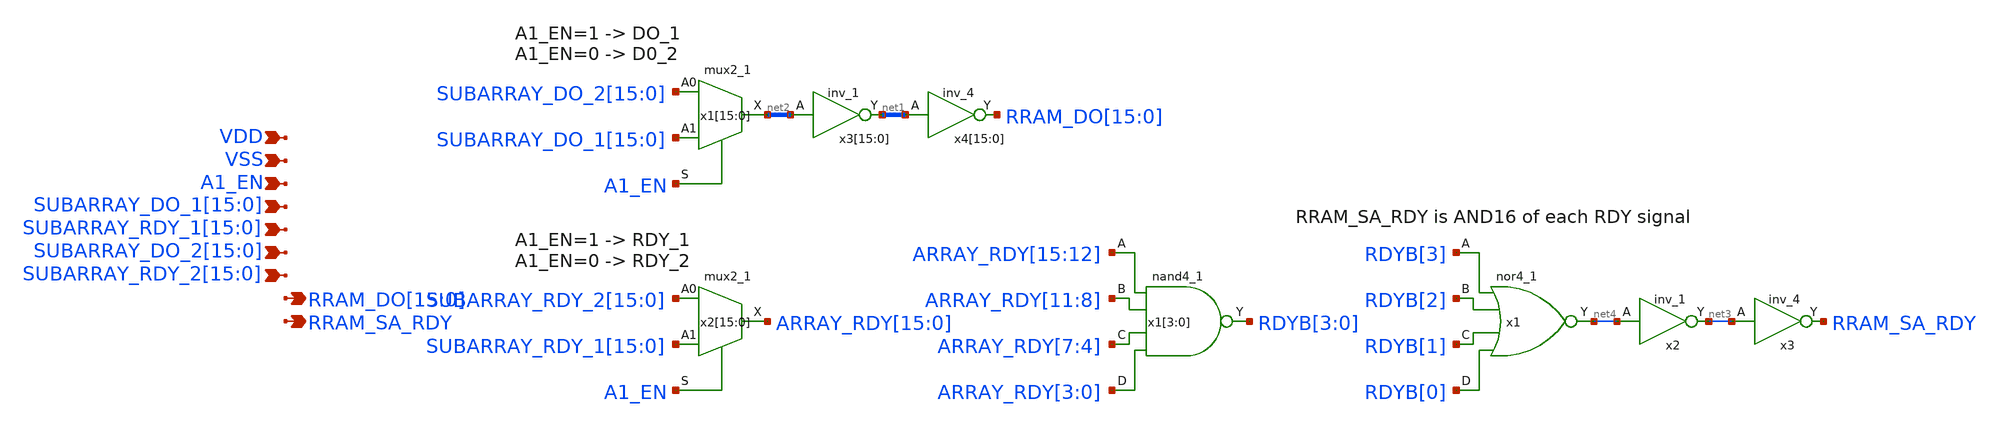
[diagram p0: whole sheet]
** sch_path: Top_Level_Array/array_output_mux.sch
**.subckt array_output_mux VDD VSS A1_EN
*+ SUBARRAY_DO_1[15],SUBARRAY_DO_1[14],SUBARRAY_DO_1[13],SUBARRAY_DO_1[12],SUBARRAY_DO_1[11],SUBARRAY_DO_1[10],SUBARRAY_DO_1[9],SUBARRAY_DO_1[8],SUBARRAY_DO_1[7],SUBARRAY_DO_1[6],SUBARRAY_DO_1[5],SUBARRAY_DO_1[4],SUBARRAY_DO_1[3],SUBARRAY_DO_1[2],SUBARRAY_DO_1[1],SUBARRAY_DO_1[0]
*+ SUBARRAY_RDY_1[15],SUBARRAY_RDY_1[14],SUBARRAY_RDY_1[13],SUBARRAY_RDY_1[12],SUBARRAY_RDY_1[11],SUBARRAY_RDY_1[10],SUBARRAY_RDY_1[9],SUBARRAY_RDY_1[8],SUBARRAY_RDY_1[7],SUBARRAY_RDY_1[6],SUBARRAY_RDY_1[5],SUBARRAY_RDY_1[4],SUBARRAY_RDY_1[3],SUBARRAY_RDY_1[2],SUBARRAY_RDY_1[1],SUBARRAY_RDY_1[0]
*+ SUBARRAY_DO_2[15],SUBARRAY_DO_2[14],SUBARRAY_DO_2[13],SUBARRAY_DO_2[12],SUBARRAY_DO_2[11],SUBARRAY_DO_2[10],SUBARRAY_DO_2[9],SUBARRAY_DO_2[8],SUBARRAY_DO_2[7],SUBARRAY_DO_2[6],SUBARRAY_DO_2[5],SUBARRAY_DO_2[4],SUBARRAY_DO_2[3],SUBARRAY_DO_2[2],SUBARRAY_DO_2[1],SUBARRAY_DO_2[0]
*+ SUBARRAY_RDY_2[15],SUBARRAY_RDY_2[14],SUBARRAY_RDY_2[13],SUBARRAY_RDY_2[12],SUBARRAY_RDY_2[11],SUBARRAY_RDY_2[10],SUBARRAY_RDY_2[9],SUBARRAY_RDY_2[8],SUBARRAY_RDY_2[7],SUBARRAY_RDY_2[6],SUBARRAY_RDY_2[5],SUBARRAY_RDY_2[4],SUBARRAY_RDY_2[3],SUBARRAY_RDY_2[2],SUBARRAY_RDY_2[1],SUBARRAY_RDY_2[0]
*+ RRAM_DO[15],RRAM_DO[14],RRAM_DO[13],RRAM_DO[12],RRAM_DO[11],RRAM_DO[10],RRAM_DO[9],RRAM_DO[8],RRAM_DO[7],RRAM_DO[6],RRAM_DO[5],RRAM_DO[4],RRAM_DO[3],RRAM_DO[2],RRAM_DO[1],RRAM_DO[0] RRAM_SA_RDY
*.ipin VDD
*.ipin VSS
*.ipin A1_EN
*.ipin
*+ SUBARRAY_DO_1[15],SUBARRAY_DO_1[14],SUBARRAY_DO_1[13],SUBARRAY_DO_1[12],SUBARRAY_DO_1[11],SUBARRAY_DO_1[10],SUBARRAY_DO_1[9],SUBARRAY_DO_1[8],SUBARRAY_DO_1[7],SUBARRAY_DO_1[6],SUBARRAY_DO_1[5],SUBARRAY_DO_1[4],SUBARRAY_DO_1[3],SUBARRAY_DO_1[2],SUBARRAY_DO_1[1],SUBARRAY_DO_1[0]
*.ipin
*+ SUBARRAY_RDY_1[15],SUBARRAY_RDY_1[14],SUBARRAY_RDY_1[13],SUBARRAY_RDY_1[12],SUBARRAY_RDY_1[11],SUBARRAY_RDY_1[10],SUBARRAY_RDY_1[9],SUBARRAY_RDY_1[8],SUBARRAY_RDY_1[7],SUBARRAY_RDY_1[6],SUBARRAY_RDY_1[5],SUBARRAY_RDY_1[4],SUBARRAY_RDY_1[3],SUBARRAY_RDY_1[2],SUBARRAY_RDY_1[1],SUBARRAY_RDY_1[0]
*.ipin
*+ SUBARRAY_DO_2[15],SUBARRAY_DO_2[14],SUBARRAY_DO_2[13],SUBARRAY_DO_2[12],SUBARRAY_DO_2[11],SUBARRAY_DO_2[10],SUBARRAY_DO_2[9],SUBARRAY_DO_2[8],SUBARRAY_DO_2[7],SUBARRAY_DO_2[6],SUBARRAY_DO_2[5],SUBARRAY_DO_2[4],SUBARRAY_DO_2[3],SUBARRAY_DO_2[2],SUBARRAY_DO_2[1],SUBARRAY_DO_2[0]
*.ipin
*+ SUBARRAY_RDY_2[15],SUBARRAY_RDY_2[14],SUBARRAY_RDY_2[13],SUBARRAY_RDY_2[12],SUBARRAY_RDY_2[11],SUBARRAY_RDY_2[10],SUBARRAY_RDY_2[9],SUBARRAY_RDY_2[8],SUBARRAY_RDY_2[7],SUBARRAY_RDY_2[6],SUBARRAY_RDY_2[5],SUBARRAY_RDY_2[4],SUBARRAY_RDY_2[3],SUBARRAY_RDY_2[2],SUBARRAY_RDY_2[1],SUBARRAY_RDY_2[0]
*.opin
*+ RRAM_DO[15],RRAM_DO[14],RRAM_DO[13],RRAM_DO[12],RRAM_DO[11],RRAM_DO[10],RRAM_DO[9],RRAM_DO[8],RRAM_DO[7],RRAM_DO[6],RRAM_DO[5],RRAM_DO[4],RRAM_DO[3],RRAM_DO[2],RRAM_DO[1],RRAM_DO[0]
*.opin RRAM_SA_RDY
x1[15] SUBARRAY_DO_2[15] SUBARRAY_DO_1[15] A1_EN VSS VSS VDD VDD net2[15] sky130_fd_sc_hd__mux2_1
x1[14] SUBARRAY_DO_2[14] SUBARRAY_DO_1[14] A1_EN VSS VSS VDD VDD net2[14] sky130_fd_sc_hd__mux2_1
x1[13] SUBARRAY_DO_2[13] SUBARRAY_DO_1[13] A1_EN VSS VSS VDD VDD net2[13] sky130_fd_sc_hd__mux2_1
x1[12] SUBARRAY_DO_2[12] SUBARRAY_DO_1[12] A1_EN VSS VSS VDD VDD net2[12] sky130_fd_sc_hd__mux2_1
x1[11] SUBARRAY_DO_2[11] SUBARRAY_DO_1[11] A1_EN VSS VSS VDD VDD net2[11] sky130_fd_sc_hd__mux2_1
x1[10] SUBARRAY_DO_2[10] SUBARRAY_DO_1[10] A1_EN VSS VSS VDD VDD net2[10] sky130_fd_sc_hd__mux2_1
x1[9] SUBARRAY_DO_2[9] SUBARRAY_DO_1[9] A1_EN VSS VSS VDD VDD net2[9] sky130_fd_sc_hd__mux2_1
x1[8] SUBARRAY_DO_2[8] SUBARRAY_DO_1[8] A1_EN VSS VSS VDD VDD net2[8] sky130_fd_sc_hd__mux2_1
x1[7] SUBARRAY_DO_2[7] SUBARRAY_DO_1[7] A1_EN VSS VSS VDD VDD net2[7] sky130_fd_sc_hd__mux2_1
x1[6] SUBARRAY_DO_2[6] SUBARRAY_DO_1[6] A1_EN VSS VSS VDD VDD net2[6] sky130_fd_sc_hd__mux2_1
x1[5] SUBARRAY_DO_2[5] SUBARRAY_DO_1[5] A1_EN VSS VSS VDD VDD net2[5] sky130_fd_sc_hd__mux2_1
x1[4] SUBARRAY_DO_2[4] SUBARRAY_DO_1[4] A1_EN VSS VSS VDD VDD net2[4] sky130_fd_sc_hd__mux2_1
x1[3] SUBARRAY_DO_2[3] SUBARRAY_DO_1[3] A1_EN VSS VSS VDD VDD net2[3] sky130_fd_sc_hd__mux2_1
x1[2] SUBARRAY_DO_2[2] SUBARRAY_DO_1[2] A1_EN VSS VSS VDD VDD net2[2] sky130_fd_sc_hd__mux2_1
x1[1] SUBARRAY_DO_2[1] SUBARRAY_DO_1[1] A1_EN VSS VSS VDD VDD net2[1] sky130_fd_sc_hd__mux2_1
x1[0] SUBARRAY_DO_2[0] SUBARRAY_DO_1[0] A1_EN VSS VSS VDD VDD net2[0] sky130_fd_sc_hd__mux2_1
x2[15] SUBARRAY_RDY_2[15] SUBARRAY_RDY_1[15] A1_EN VSS VSS VDD VDD ARRAY_RDY[15]
+ sky130_fd_sc_hd__mux2_1
x2[14] SUBARRAY_RDY_2[14] SUBARRAY_RDY_1[14] A1_EN VSS VSS VDD VDD ARRAY_RDY[14]
+ sky130_fd_sc_hd__mux2_1
x2[13] SUBARRAY_RDY_2[13] SUBARRAY_RDY_1[13] A1_EN VSS VSS VDD VDD ARRAY_RDY[13]
+ sky130_fd_sc_hd__mux2_1
x2[12] SUBARRAY_RDY_2[12] SUBARRAY_RDY_1[12] A1_EN VSS VSS VDD VDD ARRAY_RDY[12]
+ sky130_fd_sc_hd__mux2_1
x2[11] SUBARRAY_RDY_2[11] SUBARRAY_RDY_1[11] A1_EN VSS VSS VDD VDD ARRAY_RDY[11]
+ sky130_fd_sc_hd__mux2_1
x2[10] SUBARRAY_RDY_2[10] SUBARRAY_RDY_1[10] A1_EN VSS VSS VDD VDD ARRAY_RDY[10]
+ sky130_fd_sc_hd__mux2_1
x2[9] SUBARRAY_RDY_2[9] SUBARRAY_RDY_1[9] A1_EN VSS VSS VDD VDD ARRAY_RDY[9] sky130_fd_sc_hd__mux2_1
x2[8] SUBARRAY_RDY_2[8] SUBARRAY_RDY_1[8] A1_EN VSS VSS VDD VDD ARRAY_RDY[8] sky130_fd_sc_hd__mux2_1
x2[7] SUBARRAY_RDY_2[7] SUBARRAY_RDY_1[7] A1_EN VSS VSS VDD VDD ARRAY_RDY[7] sky130_fd_sc_hd__mux2_1
x2[6] SUBARRAY_RDY_2[6] SUBARRAY_RDY_1[6] A1_EN VSS VSS VDD VDD ARRAY_RDY[6] sky130_fd_sc_hd__mux2_1
x2[5] SUBARRAY_RDY_2[5] SUBARRAY_RDY_1[5] A1_EN VSS VSS VDD VDD ARRAY_RDY[5] sky130_fd_sc_hd__mux2_1
x2[4] SUBARRAY_RDY_2[4] SUBARRAY_RDY_1[4] A1_EN VSS VSS VDD VDD ARRAY_RDY[4] sky130_fd_sc_hd__mux2_1
x2[3] SUBARRAY_RDY_2[3] SUBARRAY_RDY_1[3] A1_EN VSS VSS VDD VDD ARRAY_RDY[3] sky130_fd_sc_hd__mux2_1
x2[2] SUBARRAY_RDY_2[2] SUBARRAY_RDY_1[2] A1_EN VSS VSS VDD VDD ARRAY_RDY[2] sky130_fd_sc_hd__mux2_1
x2[1] SUBARRAY_RDY_2[1] SUBARRAY_RDY_1[1] A1_EN VSS VSS VDD VDD ARRAY_RDY[1] sky130_fd_sc_hd__mux2_1
x2[0] SUBARRAY_RDY_2[0] SUBARRAY_RDY_1[0] A1_EN VSS VSS VDD VDD ARRAY_RDY[0] sky130_fd_sc_hd__mux2_1
x3[15] net2[15] VSS VSS VDD VDD net1[15] sky130_fd_sc_hd__inv_1
x3[14] net2[14] VSS VSS VDD VDD net1[14] sky130_fd_sc_hd__inv_1
x3[13] net2[13] VSS VSS VDD VDD net1[13] sky130_fd_sc_hd__inv_1
x3[12] net2[12] VSS VSS VDD VDD net1[12] sky130_fd_sc_hd__inv_1
x3[11] net2[11] VSS VSS VDD VDD net1[11] sky130_fd_sc_hd__inv_1
x3[10] net2[10] VSS VSS VDD VDD net1[10] sky130_fd_sc_hd__inv_1
x3[9] net2[9] VSS VSS VDD VDD net1[9] sky130_fd_sc_hd__inv_1
x3[8] net2[8] VSS VSS VDD VDD net1[8] sky130_fd_sc_hd__inv_1
x3[7] net2[7] VSS VSS VDD VDD net1[7] sky130_fd_sc_hd__inv_1
x3[6] net2[6] VSS VSS VDD VDD net1[6] sky130_fd_sc_hd__inv_1
x3[5] net2[5] VSS VSS VDD VDD net1[5] sky130_fd_sc_hd__inv_1
x3[4] net2[4] VSS VSS VDD VDD net1[4] sky130_fd_sc_hd__inv_1
x3[3] net2[3] VSS VSS VDD VDD net1[3] sky130_fd_sc_hd__inv_1
x3[2] net2[2] VSS VSS VDD VDD net1[2] sky130_fd_sc_hd__inv_1
x3[1] net2[1] VSS VSS VDD VDD net1[1] sky130_fd_sc_hd__inv_1
x3[0] net2[0] VSS VSS VDD VDD net1[0] sky130_fd_sc_hd__inv_1
x4[15] net1[15] VSS VSS VDD VDD RRAM_DO[15] sky130_fd_sc_hd__inv_4
x4[14] net1[14] VSS VSS VDD VDD RRAM_DO[14] sky130_fd_sc_hd__inv_4
x4[13] net1[13] VSS VSS VDD VDD RRAM_DO[13] sky130_fd_sc_hd__inv_4
x4[12] net1[12] VSS VSS VDD VDD RRAM_DO[12] sky130_fd_sc_hd__inv_4
x4[11] net1[11] VSS VSS VDD VDD RRAM_DO[11] sky130_fd_sc_hd__inv_4
x4[10] net1[10] VSS VSS VDD VDD RRAM_DO[10] sky130_fd_sc_hd__inv_4
x4[9] net1[9] VSS VSS VDD VDD RRAM_DO[9] sky130_fd_sc_hd__inv_4
x4[8] net1[8] VSS VSS VDD VDD RRAM_DO[8] sky130_fd_sc_hd__inv_4
x4[7] net1[7] VSS VSS VDD VDD RRAM_DO[7] sky130_fd_sc_hd__inv_4
x4[6] net1[6] VSS VSS VDD VDD RRAM_DO[6] sky130_fd_sc_hd__inv_4
x4[5] net1[5] VSS VSS VDD VDD RRAM_DO[5] sky130_fd_sc_hd__inv_4
x4[4] net1[4] VSS VSS VDD VDD RRAM_DO[4] sky130_fd_sc_hd__inv_4
x4[3] net1[3] VSS VSS VDD VDD RRAM_DO[3] sky130_fd_sc_hd__inv_4
x4[2] net1[2] VSS VSS VDD VDD RRAM_DO[2] sky130_fd_sc_hd__inv_4
x4[1] net1[1] VSS VSS VDD VDD RRAM_DO[1] sky130_fd_sc_hd__inv_4
x4[0] net1[0] VSS VSS VDD VDD RRAM_DO[0] sky130_fd_sc_hd__inv_4
x1[3] ARRAY_RDY[15] ARRAY_RDY[11] ARRAY_RDY[7] ARRAY_RDY[3] VSS VSS VDD VDD RDYB[3]
+ sky130_fd_sc_hd__nand4_1
x1[2] ARRAY_RDY[14] ARRAY_RDY[10] ARRAY_RDY[6] ARRAY_RDY[2] VSS VSS VDD VDD RDYB[2]
+ sky130_fd_sc_hd__nand4_1
x1[1] ARRAY_RDY[13] ARRAY_RDY[9] ARRAY_RDY[5] ARRAY_RDY[1] VSS VSS VDD VDD RDYB[1]
+ sky130_fd_sc_hd__nand4_1
x1[0] ARRAY_RDY[12] ARRAY_RDY[8] ARRAY_RDY[4] ARRAY_RDY[0] VSS VSS VDD VDD RDYB[0]
+ sky130_fd_sc_hd__nand4_1
x1 RDYB[3] RDYB[2] RDYB[1] RDYB[0] VSS VSS VDD VDD net4 sky130_fd_sc_hd__nor4_1
x2 net4 VSS VSS VDD VDD net3 sky130_fd_sc_hd__inv_1
x3 net3 VSS VSS VDD VDD RRAM_SA_RDY sky130_fd_sc_hd__inv_4
**.ends
.end
